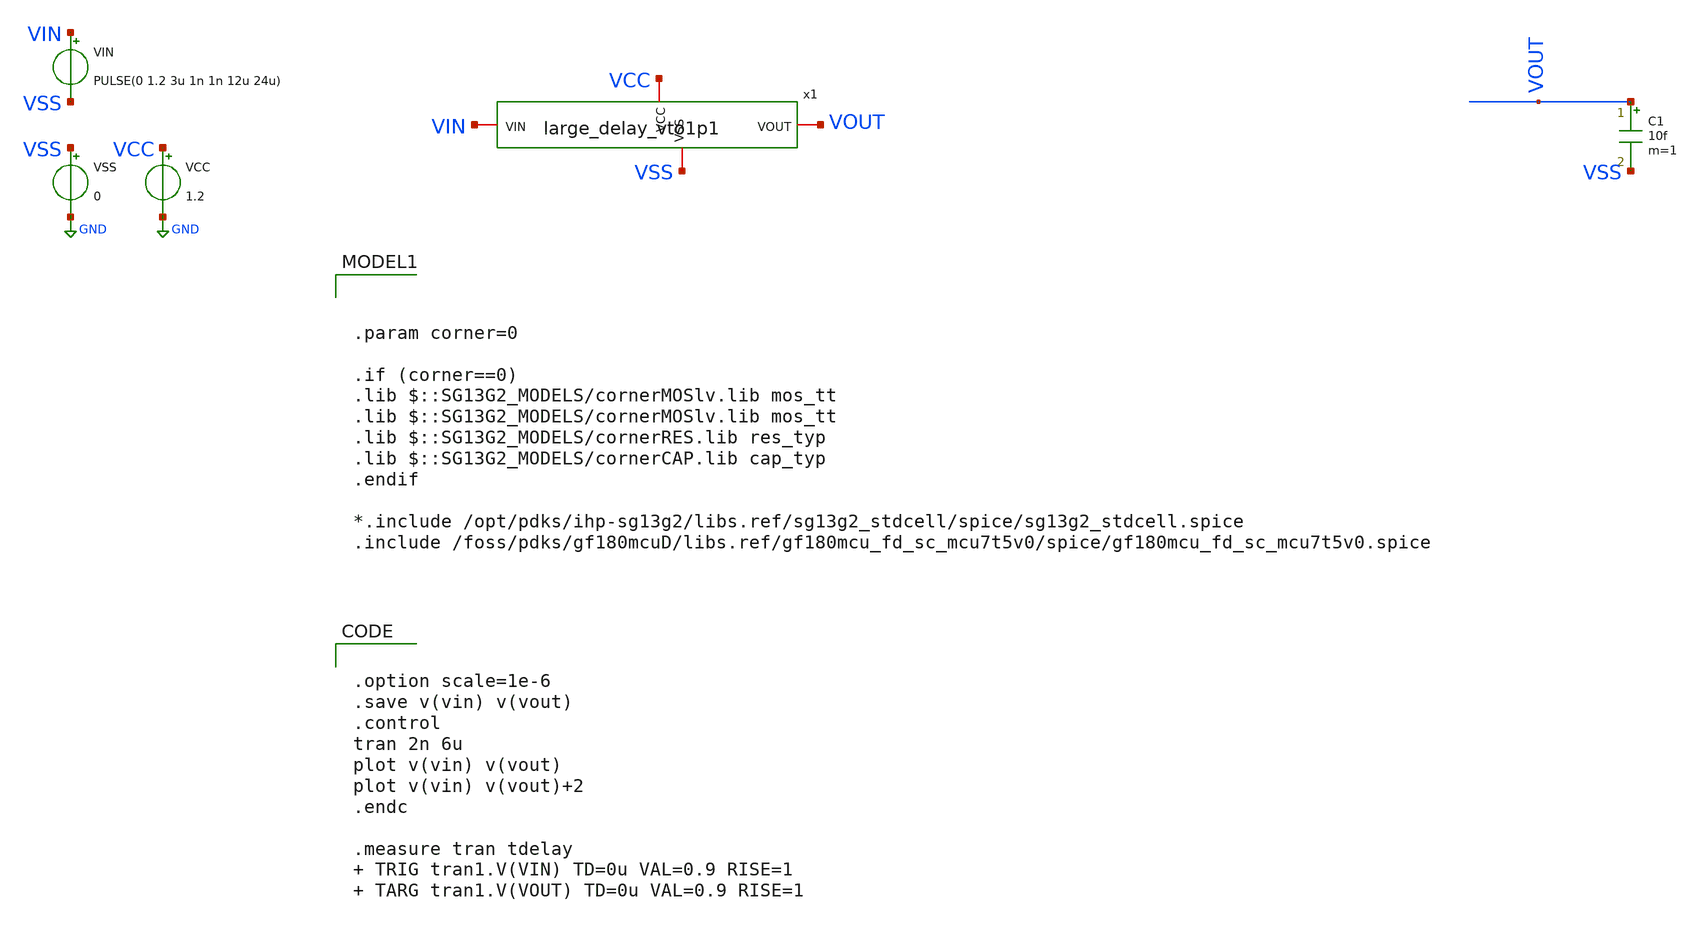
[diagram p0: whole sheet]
** sch_path: xschem/large_delay/tb_largedelay_vto1p1.sch
**.subckt tb_largedelay_vto1p1
VCC VCC GND 1.2
VSS VSS GND 0
VIN VIN VSS PULSE(0 1.2 3u 1n 1n 12u 24u)
C1 VOUT VSS 10f m=1
x1 VCC VSS VIN VOUT large_delay_vto1p1
**** begin user architecture code


.option scale=1e-6
.save v(vin) v(vout)
.control
tran 2n 6u
plot v(vin) v(vout)
plot v(vin) v(vout)+2
.endc

.measure tran tdelay  TRIG tran1.V(VIN) TD=0u VAL=0.9 RISE=1  TARG tran1.V(VOUT) TD=0u VAL=0.9
+ RISE=1






.param corner=0

.if (corner==0)
.lib $::SG13G2_MODELS/cornerMOSlv.lib mos_tt
.lib $::SG13G2_MODELS/cornerMOSlv.lib mos_tt
.lib $::SG13G2_MODELS/cornerRES.lib res_typ
.lib $::SG13G2_MODELS/cornerCAP.lib cap_typ
.endif

*.include /opt/pdks/ihp-sg13g2/libs.ref/sg13g2_stdcell/spice/sg13g2_stdcell.spice
.include /foss/pdks/gf180mcuD/libs.ref/gf180mcu_fd_sc_mcu7t5v0/spice/gf180mcu_fd_sc_mcu7t5v0.spice

**** end user architecture code
**.ends
.GLOBAL GND
.end
